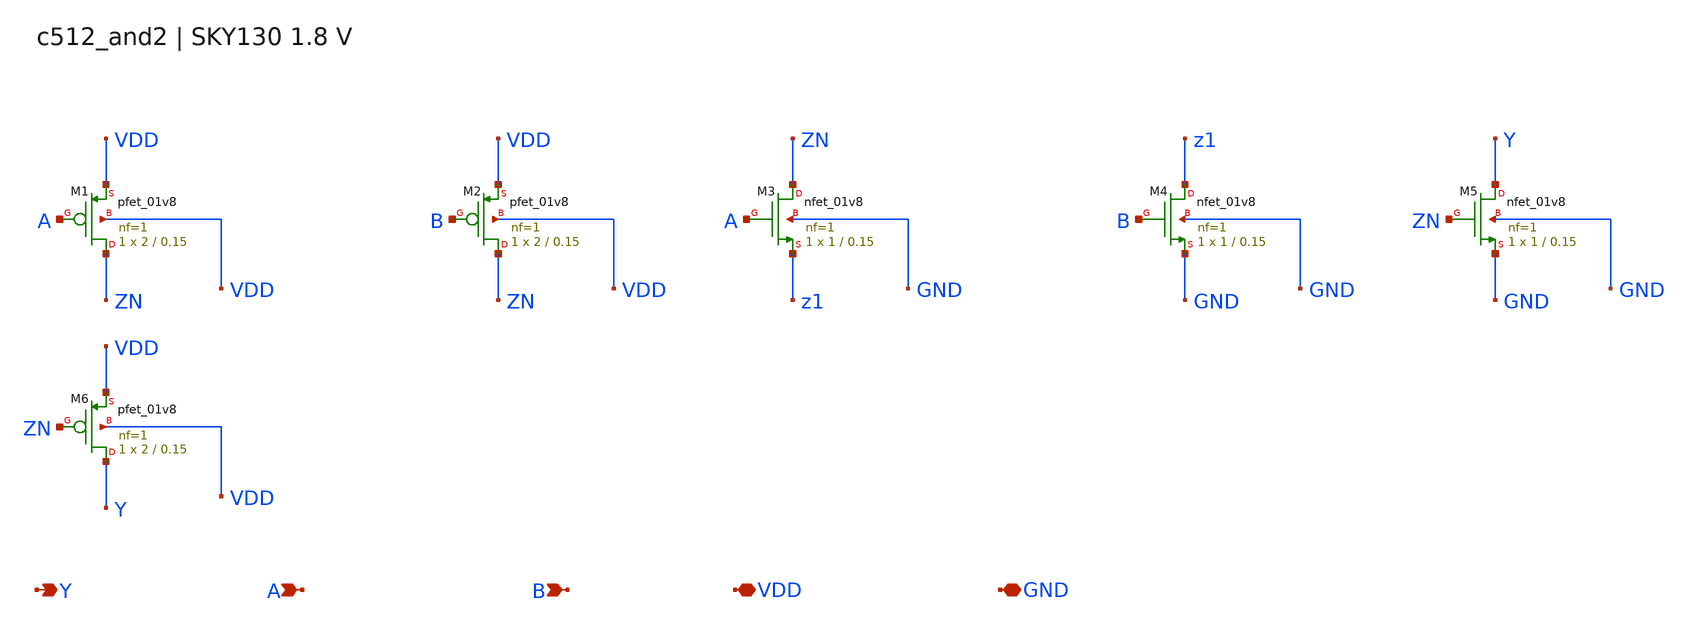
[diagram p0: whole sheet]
** sch_path: c512_and2.sch
**.subckt c512_and2 Y A B VDD GND
*.opin Y
*.ipin A
*.ipin B
*.iopin VDD
*.iopin GND
XM1 ZN A VDD VDD sky130_fd_pr__pfet_01v8 L=0.15 W=2 nf=1 ad=0.58 as=0.58 pd=4.58 ps=4.58 nrd=0.145
+ nrs=0.145 sa=0 sb=0 sd=0 mult=1 m=1
XM2 ZN B VDD VDD sky130_fd_pr__pfet_01v8 L=0.15 W=2 nf=1 ad=0.58 as=0.58 pd=4.58 ps=4.58 nrd=0.145
+ nrs=0.145 sa=0 sb=0 sd=0 mult=1 m=1
XM3 ZN A z1 GND sky130_fd_pr__nfet_01v8 L=0.15 W=1 nf=1 ad=0.29 as=0.29 pd=2.58 ps=2.58 nrd=0.29
+ nrs=0.29 sa=0 sb=0 sd=0 mult=1 m=1
XM4 z1 B GND GND sky130_fd_pr__nfet_01v8 L=0.15 W=1 nf=1 ad=0.29 as=0.29 pd=2.58 ps=2.58 nrd=0.29
+ nrs=0.29 sa=0 sb=0 sd=0 mult=1 m=1
XM5 Y ZN GND GND sky130_fd_pr__nfet_01v8 L=0.15 W=1 nf=1 ad=0.29 as=0.29 pd=2.58 ps=2.58 nrd=0.29
+ nrs=0.29 sa=0 sb=0 sd=0 mult=1 m=1
XM6 Y ZN VDD VDD sky130_fd_pr__pfet_01v8 L=0.15 W=2 nf=1 ad=0.58 as=0.58 pd=4.58 ps=4.58 nrd=0.145
+ nrs=0.145 sa=0 sb=0 sd=0 mult=1 m=1
**.ends
.end
